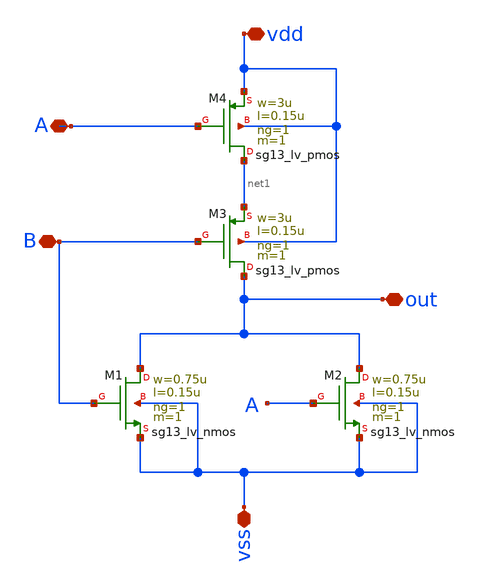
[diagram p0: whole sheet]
** sch_path: design/blocks/nor2/schematic/nor2.sch
**.subckt nor2 vdd A B vss out
*.iopin vdd
*.iopin A
*.iopin B
*.iopin vss
*.iopin out
XM1 out B vss vss sg13_lv_nmos w=0.75u l=0.15u ng=1 m=1 mm_ok=1
XM2 out A vss vss sg13_lv_nmos w=0.75u l=0.15u ng=1 m=1 mm_ok=1
XM3 out B net1 vdd sg13_lv_pmos w=3u l=0.15u ng=1 m=1 mm_ok=1
XM4 net1 A vdd vdd sg13_lv_pmos w=3u l=0.15u ng=1 m=1 mm_ok=1
**.ends
.end
